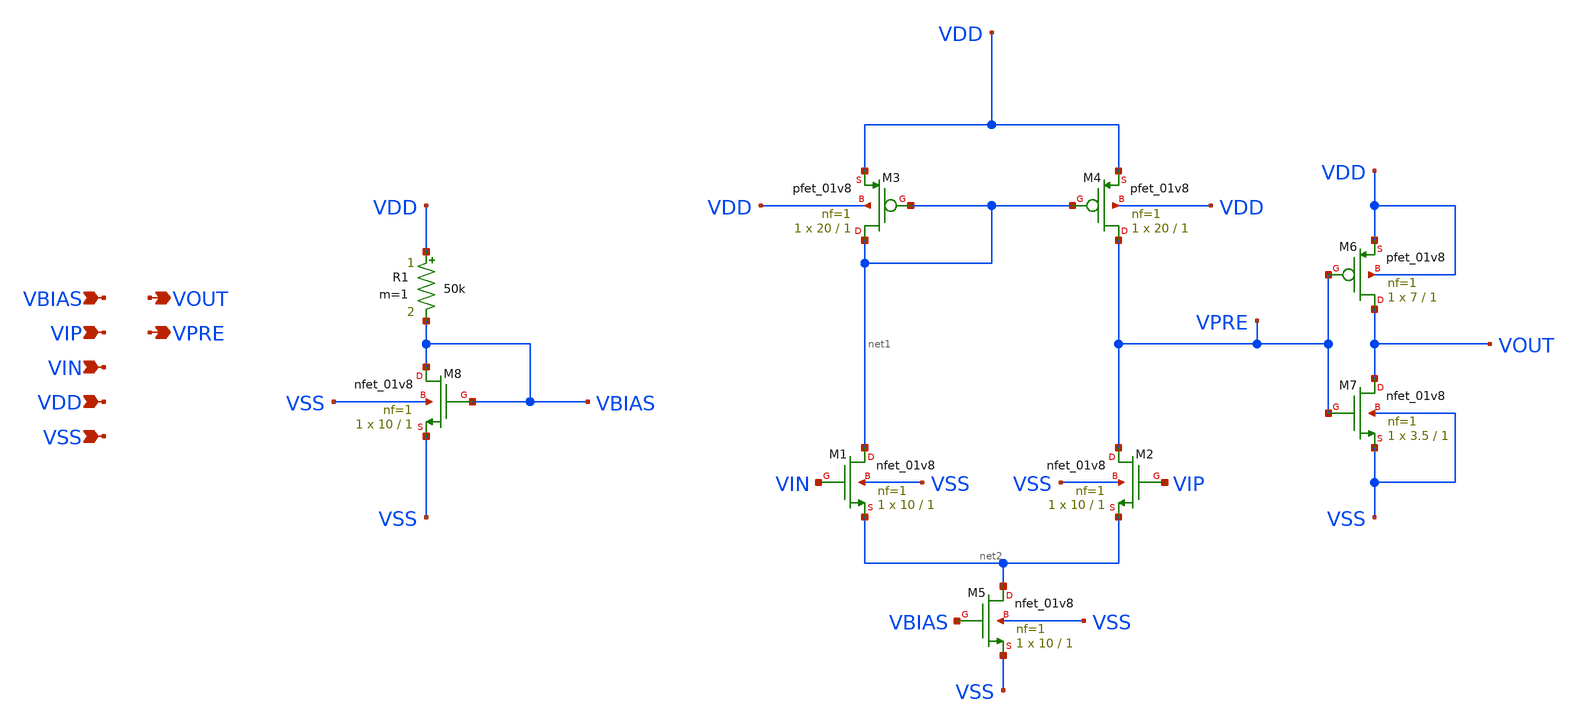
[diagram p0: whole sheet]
** sch_path: xsch/comparator.sch
**.subckt comparator VIP VIN VDD VSS VBIAS VOUT VPRE
*.ipin VIP
*.ipin VIN
*.ipin VDD
*.ipin VSS
*.ipin VBIAS
*.opin VOUT
*.opin VPRE
XM1 net1 VIN net2 VSS sky130_fd_pr__nfet_01v8 L=1 W=10 nf=1 ad='int((1 + 1)/2) * 10 / 1 * 0.29' as='int((1 + 2)/2) * 10 / 1 * 0.29'
+ pd='2*int((1 + 1)/2) * (10 / 1 + 0.29)' ps='2*int((1 + 2)/2) * (10 / 1 + 0.29)' nrd='0.29 / 10 ' nrs='0.29 / 10 '
+ sa=0 sb=0 sd=0 mult=1 m=1
XM2 VPRE VIP net2 VSS sky130_fd_pr__nfet_01v8 L=1 W=10 nf=1 ad='int((1 + 1)/2) * 10 / 1 * 0.29' as='int((1 + 2)/2) * 10 / 1 * 0.29'
+ pd='2*int((1 + 1)/2) * (10 / 1 + 0.29)' ps='2*int((1 + 2)/2) * (10 / 1 + 0.29)' nrd='0.29 / 10 ' nrs='0.29 / 10 '
+ sa=0 sb=0 sd=0 mult=1 m=1
XM4 VPRE net1 VDD VDD sky130_fd_pr__pfet_01v8 L=1 W=20 nf=1 ad='int((1 + 1)/2) * 20 / 1 * 0.29' as='int((1 + 2)/2) * 20 / 1 * 0.29'
+ pd='2*int((1 + 1)/2) * (20 / 1 + 0.29)' ps='2*int((1 + 2)/2) * (20 / 1 + 0.29)' nrd='0.29 / 20 ' nrs='0.29 / 20 '
+ sa=0 sb=0 sd=0 mult=1 m=1
XM3 net1 net1 VDD VDD sky130_fd_pr__pfet_01v8 L=1 W=20 nf=1 ad='int((1 + 1)/2) * 20 / 1 * 0.29' as='int((1 + 2)/2) * 20 / 1 * 0.29'
+ pd='2*int((1 + 1)/2) * (20 / 1 + 0.29)' ps='2*int((1 + 2)/2) * (20 / 1 + 0.29)' nrd='0.29 / 20 ' nrs='0.29 / 20 '
+ sa=0 sb=0 sd=0 mult=1 m=1
XM5 net2 VBIAS VSS VSS sky130_fd_pr__nfet_01v8 L=1 W=10 nf=1 ad='int((1 + 1)/2) * 10 / 1 * 0.29' as='int((1 + 2)/2) * 10 / 1 * 0.29'
+ pd='2*int((1 + 1)/2) * (10 / 1 + 0.29)' ps='2*int((1 + 2)/2) * (10 / 1 + 0.29)' nrd='0.29 / 10 ' nrs='0.29 / 10 '
+ sa=0 sb=0 sd=0 mult=1 m=1
XM6 VOUT VPRE VDD VDD sky130_fd_pr__pfet_01v8 L=1 W=7 nf=1 ad='int((1 + 1)/2) * 7 / 1 * 0.29' as='int((1 + 2)/2) * 7 / 1 * 0.29'
+ pd='2*int((1 + 1)/2) * (7 / 1 + 0.29)' ps='2*int((1 + 2)/2) * (7 / 1 + 0.29)' nrd='0.29 / 7 ' nrs='0.29 / 7 '
+ sa=0 sb=0 sd=0 mult=1 m=1
XM7 VOUT VPRE VSS VSS sky130_fd_pr__nfet_01v8 L=1 W=3.5 nf=1 ad='int((1 + 1)/2) * 3.5 / 1 * 0.29' as='int((1 + 2)/2) * 3.5 / 1 * 0.29'
+ pd='2*int((1 + 1)/2) * (3.5 / 1 + 0.29)' ps='2*int((1 + 2)/2) * (3.5 / 1 + 0.29)' nrd='0.29 / 3.5 ' nrs='0.29 / 3.5 '
+ sa=0 sb=0 sd=0 mult=1 m=1
XM8 VBIAS VBIAS VSS VSS sky130_fd_pr__nfet_01v8 L=1 W=10 nf=1 ad='int((1 + 1)/2) * 10 / 1 * 0.29' as='int((1 + 2)/2) * 10 / 1 * 0.29'
+ pd='2*int((1 + 1)/2) * (10 / 1 + 0.29)' ps='2*int((1 + 2)/2) * (10 / 1 + 0.29)' nrd='0.29 / 10 ' nrs='0.29 / 10 '
+ sa=0 sb=0 sd=0 mult=1 m=1
R1 VDD VBIAS 50k m=1
**.ends
.end
